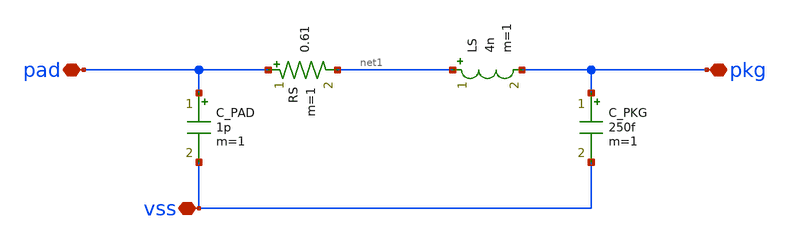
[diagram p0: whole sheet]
** sch_path: designs/libs/core_analog/asc_bond_wire/asc_bond_wire.sch
**.subckt asc_bond_wire vss pad pkg
*.iopin vss
*.iopin pad
*.iopin pkg
C_PAD pad vss 1p m=1
LS net1 pkg 4n m=1
C_PKG pkg vss 250f m=1
RS pad net1 0.61 m=1
**.ends
.end
